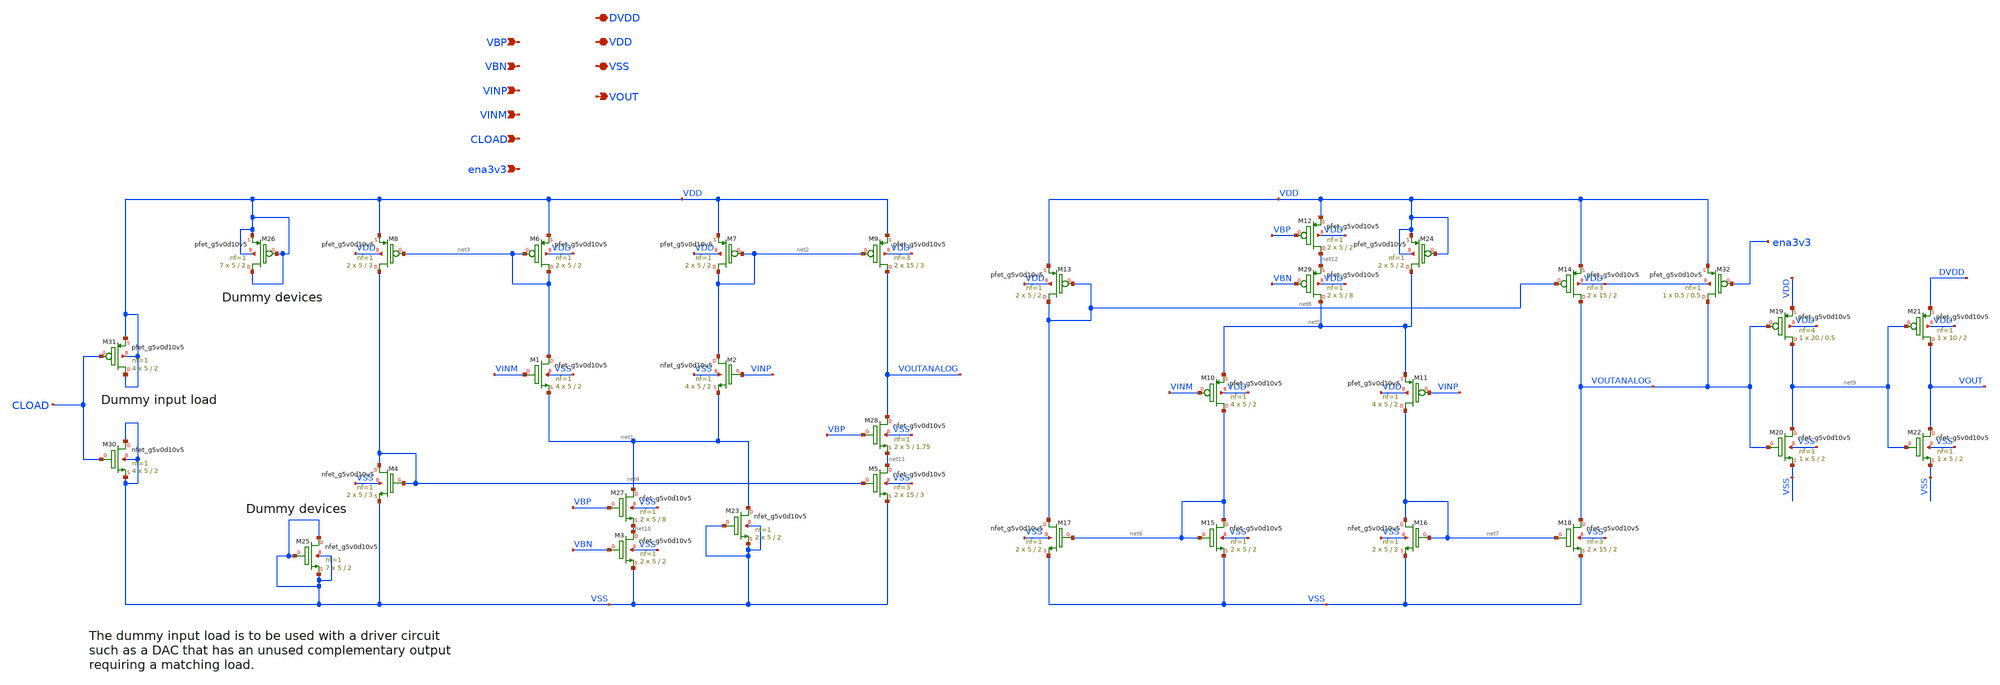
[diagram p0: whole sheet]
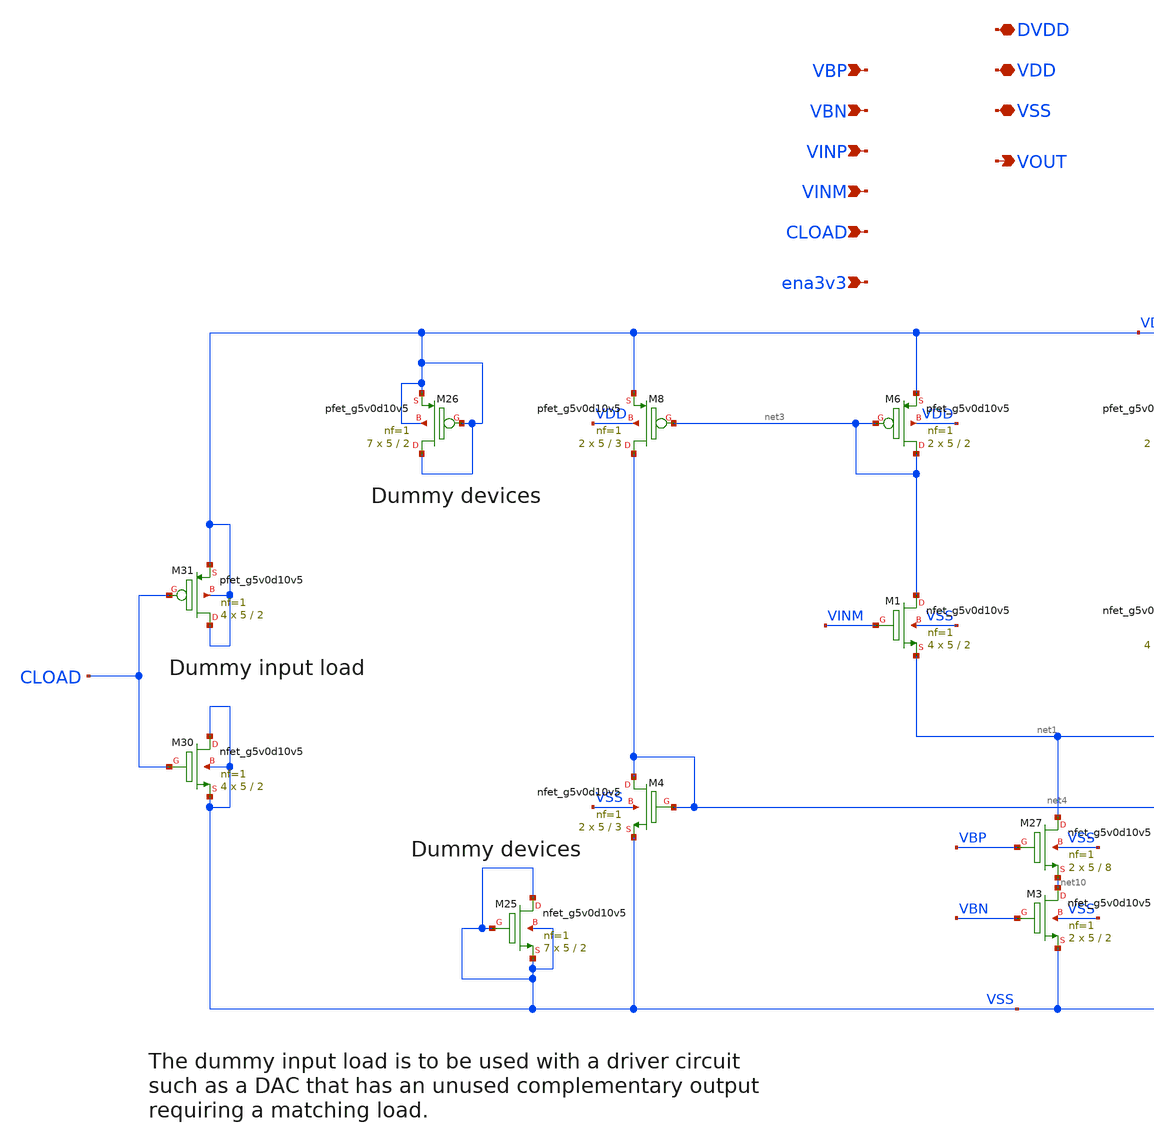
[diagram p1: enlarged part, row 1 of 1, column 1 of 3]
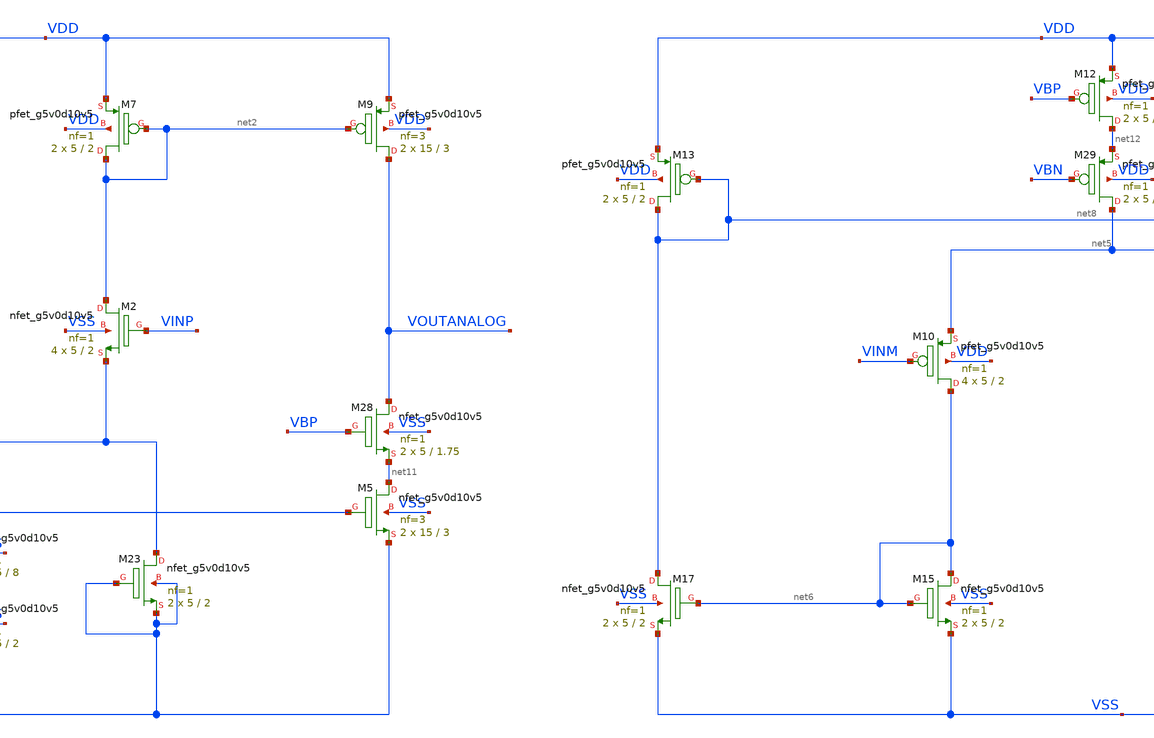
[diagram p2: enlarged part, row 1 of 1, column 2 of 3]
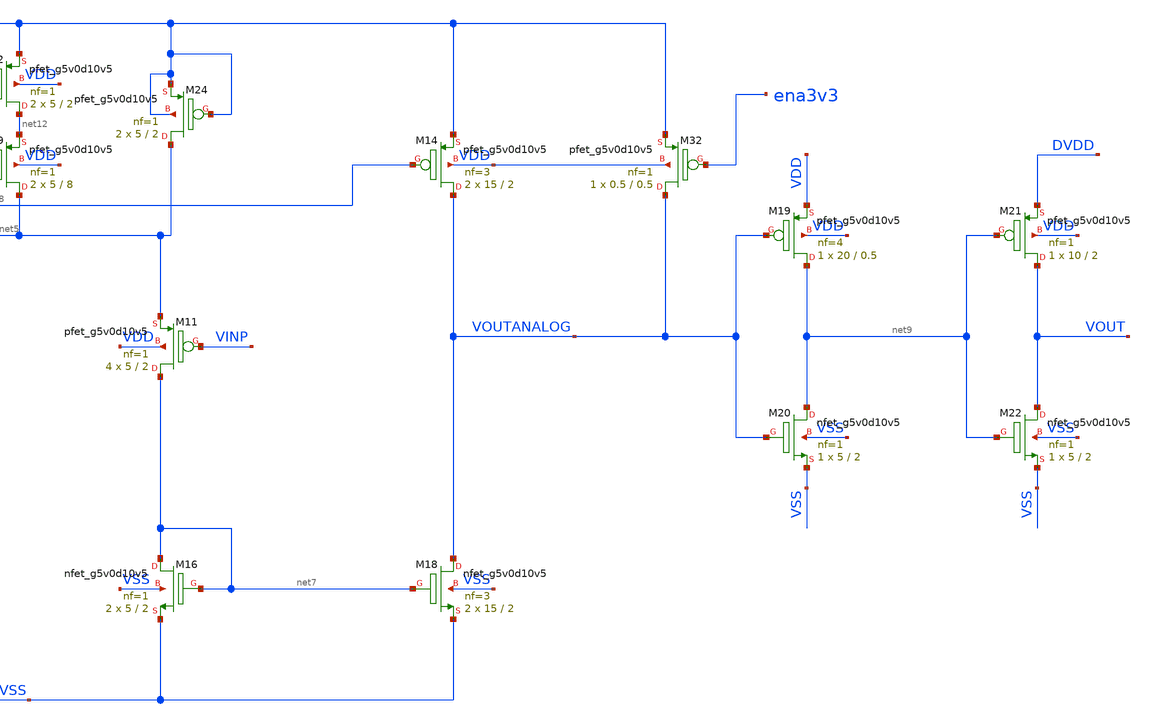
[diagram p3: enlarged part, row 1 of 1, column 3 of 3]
** sch_path: xschem/comparator_core_cload.sch
**.subckt comparator_core_cload VINP VINM VBN VBP VDD VSS VOUT DVDD CLOAD ena3v3
*.ipin VINP
*.ipin VINM
*.ipin VBN
*.ipin VBP
*.iopin VDD
*.iopin VSS
*.opin VOUT
*.iopin DVDD
*.ipin CLOAD
*.ipin ena3v3
XM3 net10 VBN VSS VSS sky130_fd_pr__nfet_g5v0d10v5 L=2 W=5 nf=1 ad='int((nf+1)/2) * W/nf * 0.29' as='int((nf+2)/2) * W/nf * 0.29'
+ pd='2*int((nf+1)/2) * (W/nf + 0.29)' ps='2*int((nf+2)/2) * (W/nf + 0.29)' nrd='0.29 / W' nrs='0.29 / W'
+ sa=0 sb=0 sd=0 mult=2 m=2
XM4 net4 net4 VSS VSS sky130_fd_pr__nfet_g5v0d10v5 L=3 W=5 nf=1 ad='int((nf+1)/2) * W/nf * 0.29' as='int((nf+2)/2) * W/nf * 0.29'
+ pd='2*int((nf+1)/2) * (W/nf + 0.29)' ps='2*int((nf+2)/2) * (W/nf + 0.29)' nrd='0.29 / W' nrs='0.29 / W'
+ sa=0 sb=0 sd=0 mult=2 m=2
XM5 net11 net4 VSS VSS sky130_fd_pr__nfet_g5v0d10v5 L=3 W=15 nf=3 ad='int((nf+1)/2) * W/nf * 0.29' as='int((nf+2)/2) * W/nf * 0.29'
+ pd='2*int((nf+1)/2) * (W/nf + 0.29)' ps='2*int((nf+2)/2) * (W/nf + 0.29)' nrd='0.29 / W' nrs='0.29 / W'
+ sa=0 sb=0 sd=0 mult=2 m=2
XM6 net3 net3 VDD VDD sky130_fd_pr__pfet_g5v0d10v5 L=2 W=5 nf=1 ad='int((nf+1)/2) * W/nf * 0.29' as='int((nf+2)/2) * W/nf * 0.29'
+ pd='2*int((nf+1)/2) * (W/nf + 0.29)' ps='2*int((nf+2)/2) * (W/nf + 0.29)' nrd='0.29 / W' nrs='0.29 / W'
+ sa=0 sb=0 sd=0 mult=2 m=2
XM7 net2 net2 VDD VDD sky130_fd_pr__pfet_g5v0d10v5 L=2 W=5 nf=1 ad='int((nf+1)/2) * W/nf * 0.29' as='int((nf+2)/2) * W/nf * 0.29'
+ pd='2*int((nf+1)/2) * (W/nf + 0.29)' ps='2*int((nf+2)/2) * (W/nf + 0.29)' nrd='0.29 / W' nrs='0.29 / W'
+ sa=0 sb=0 sd=0 mult=2 m=2
XM8 net4 net3 VDD VDD sky130_fd_pr__pfet_g5v0d10v5 L=3 W=5 nf=1 ad='int((nf+1)/2) * W/nf * 0.29' as='int((nf+2)/2) * W/nf * 0.29'
+ pd='2*int((nf+1)/2) * (W/nf + 0.29)' ps='2*int((nf+2)/2) * (W/nf + 0.29)' nrd='0.29 / W' nrs='0.29 / W'
+ sa=0 sb=0 sd=0 mult=2 m=2
XM9 VOUTANALOG net2 VDD VDD sky130_fd_pr__pfet_g5v0d10v5 L=3 W=15 nf=3 ad='int((nf+1)/2) * W/nf * 0.29'
+ as='int((nf+2)/2) * W/nf * 0.29' pd='2*int((nf+1)/2) * (W/nf + 0.29)' ps='2*int((nf+2)/2) * (W/nf + 0.29)'
+ nrd='0.29 / W' nrs='0.29 / W' sa=0 sb=0 sd=0 mult=2 m=2
XM10 net6 VINM net5 VDD sky130_fd_pr__pfet_g5v0d10v5 L=2 W=5 nf=1 ad='int((nf+1)/2) * W/nf * 0.29' as='int((nf+2)/2) * W/nf * 0.29'
+ pd='2*int((nf+1)/2) * (W/nf + 0.29)' ps='2*int((nf+2)/2) * (W/nf + 0.29)' nrd='0.29 / W' nrs='0.29 / W'
+ sa=0 sb=0 sd=0 mult=4 m=4
XM11 net7 VINP net5 VDD sky130_fd_pr__pfet_g5v0d10v5 L=2 W=5 nf=1 ad='int((nf+1)/2) * W/nf * 0.29' as='int((nf+2)/2) * W/nf * 0.29'
+ pd='2*int((nf+1)/2) * (W/nf + 0.29)' ps='2*int((nf+2)/2) * (W/nf + 0.29)' nrd='0.29 / W' nrs='0.29 / W'
+ sa=0 sb=0 sd=0 mult=4 m=4
XM12 net12 VBP VDD VDD sky130_fd_pr__pfet_g5v0d10v5 L=2 W=5 nf=1 ad='int((nf+1)/2) * W/nf * 0.29' as='int((nf+2)/2) * W/nf * 0.29'
+ pd='2*int((nf+1)/2) * (W/nf + 0.29)' ps='2*int((nf+2)/2) * (W/nf + 0.29)' nrd='0.29 / W' nrs='0.29 / W'
+ sa=0 sb=0 sd=0 mult=2 m=2
XM13 net8 net8 VDD VDD sky130_fd_pr__pfet_g5v0d10v5 L=2 W=5 nf=1 ad='int((nf+1)/2) * W/nf * 0.29' as='int((nf+2)/2) * W/nf * 0.29'
+ pd='2*int((nf+1)/2) * (W/nf + 0.29)' ps='2*int((nf+2)/2) * (W/nf + 0.29)' nrd='0.29 / W' nrs='0.29 / W'
+ sa=0 sb=0 sd=0 mult=2 m=2
XM14 VOUTANALOG net8 VDD VDD sky130_fd_pr__pfet_g5v0d10v5 L=2 W=15 nf=3 ad='int((nf+1)/2) * W/nf * 0.29'
+ as='int((nf+2)/2) * W/nf * 0.29' pd='2*int((nf+1)/2) * (W/nf + 0.29)' ps='2*int((nf+2)/2) * (W/nf + 0.29)'
+ nrd='0.29 / W' nrs='0.29 / W' sa=0 sb=0 sd=0 mult=2 m=2
XM15 net6 net6 VSS VSS sky130_fd_pr__nfet_g5v0d10v5 L=2 W=5 nf=1 ad='int((nf+1)/2) * W/nf * 0.29' as='int((nf+2)/2) * W/nf * 0.29'
+ pd='2*int((nf+1)/2) * (W/nf + 0.29)' ps='2*int((nf+2)/2) * (W/nf + 0.29)' nrd='0.29 / W' nrs='0.29 / W'
+ sa=0 sb=0 sd=0 mult=2 m=2
XM16 net7 net7 VSS VSS sky130_fd_pr__nfet_g5v0d10v5 L=2 W=5 nf=1 ad='int((nf+1)/2) * W/nf * 0.29' as='int((nf+2)/2) * W/nf * 0.29'
+ pd='2*int((nf+1)/2) * (W/nf + 0.29)' ps='2*int((nf+2)/2) * (W/nf + 0.29)' nrd='0.29 / W' nrs='0.29 / W'
+ sa=0 sb=0 sd=0 mult=2 m=2
XM17 net8 net6 VSS VSS sky130_fd_pr__nfet_g5v0d10v5 L=2 W=5 nf=1 ad='int((nf+1)/2) * W/nf * 0.29' as='int((nf+2)/2) * W/nf * 0.29'
+ pd='2*int((nf+1)/2) * (W/nf + 0.29)' ps='2*int((nf+2)/2) * (W/nf + 0.29)' nrd='0.29 / W' nrs='0.29 / W'
+ sa=0 sb=0 sd=0 mult=2 m=2
XM18 VOUTANALOG net7 VSS VSS sky130_fd_pr__nfet_g5v0d10v5 L=2 W=15 nf=3 ad='int((nf+1)/2) * W/nf * 0.29'
+ as='int((nf+2)/2) * W/nf * 0.29' pd='2*int((nf+1)/2) * (W/nf + 0.29)' ps='2*int((nf+2)/2) * (W/nf + 0.29)'
+ nrd='0.29 / W' nrs='0.29 / W' sa=0 sb=0 sd=0 mult=2 m=2
XM19 net9 VOUTANALOG VDD VDD sky130_fd_pr__pfet_g5v0d10v5 L=0.5 W=20 nf=4 ad='int((nf+1)/2) * W/nf * 0.29'
+ as='int((nf+2)/2) * W/nf * 0.29' pd='2*int((nf+1)/2) * (W/nf + 0.29)' ps='2*int((nf+2)/2) * (W/nf + 0.29)'
+ nrd='0.29 / W' nrs='0.29 / W' sa=0 sb=0 sd=0 mult=1 m=1
XM20 net9 VOUTANALOG VSS VSS sky130_fd_pr__nfet_g5v0d10v5 L=2 W=5 nf=1 ad='int((nf+1)/2) * W/nf * 0.29'
+ as='int((nf+2)/2) * W/nf * 0.29' pd='2*int((nf+1)/2) * (W/nf + 0.29)' ps='2*int((nf+2)/2) * (W/nf + 0.29)'
+ nrd='0.29 / W' nrs='0.29 / W' sa=0 sb=0 sd=0 mult=1 m=1
XM21 VOUT net9 DVDD VDD sky130_fd_pr__pfet_g5v0d10v5 L=2 W=10 nf=1 ad='int((nf+1)/2) * W/nf * 0.29' as='int((nf+2)/2) * W/nf * 0.29'
+ pd='2*int((nf+1)/2) * (W/nf + 0.29)' ps='2*int((nf+2)/2) * (W/nf + 0.29)' nrd='0.29 / W' nrs='0.29 / W'
+ sa=0 sb=0 sd=0 mult=1 m=1
XM22 VOUT net9 VSS VSS sky130_fd_pr__nfet_g5v0d10v5 L=2 W=5 nf=1 ad='int((nf+1)/2) * W/nf * 0.29' as='int((nf+2)/2) * W/nf * 0.29'
+ pd='2*int((nf+1)/2) * (W/nf + 0.29)' ps='2*int((nf+2)/2) * (W/nf + 0.29)' nrd='0.29 / W' nrs='0.29 / W'
+ sa=0 sb=0 sd=0 mult=1 m=1
XM23 net1 VSS VSS VSS sky130_fd_pr__nfet_g5v0d10v5 L=2 W=5 nf=1 ad='int((nf+1)/2) * W/nf * 0.29' as='int((nf+2)/2) * W/nf * 0.29'
+ pd='2*int((nf+1)/2) * (W/nf + 0.29)' ps='2*int((nf+2)/2) * (W/nf + 0.29)' nrd='0.29 / W' nrs='0.29 / W'
+ sa=0 sb=0 sd=0 mult=2 m=2
XM24 net5 VDD VDD VDD sky130_fd_pr__pfet_g5v0d10v5 L=2 W=5 nf=1 ad='int((nf+1)/2) * W/nf * 0.29' as='int((nf+2)/2) * W/nf * 0.29'
+ pd='2*int((nf+1)/2) * (W/nf + 0.29)' ps='2*int((nf+2)/2) * (W/nf + 0.29)' nrd='0.29 / W' nrs='0.29 / W'
+ sa=0 sb=0 sd=0 mult=2 m=2
XM25 VSS VSS VSS VSS sky130_fd_pr__nfet_g5v0d10v5 L=2 W=5 nf=1 ad='int((nf+1)/2) * W/nf * 0.29' as='int((nf+2)/2) * W/nf * 0.29'
+ pd='2*int((nf+1)/2) * (W/nf + 0.29)' ps='2*int((nf+2)/2) * (W/nf + 0.29)' nrd='0.29 / W' nrs='0.29 / W'
+ sa=0 sb=0 sd=0 mult=7 m=7
XM26 VDD VDD VDD VDD sky130_fd_pr__pfet_g5v0d10v5 L=2 W=5 nf=1 ad='int((nf+1)/2) * W/nf * 0.29' as='int((nf+2)/2) * W/nf * 0.29'
+ pd='2*int((nf+1)/2) * (W/nf + 0.29)' ps='2*int((nf+2)/2) * (W/nf + 0.29)' nrd='0.29 / W' nrs='0.29 / W'
+ sa=0 sb=0 sd=0 mult=7 m=7
XM1 net3 VINM net1 VSS sky130_fd_pr__nfet_g5v0d10v5 L=2 W=5 nf=1 ad='int((nf+1)/2) * W/nf * 0.29' as='int((nf+2)/2) * W/nf * 0.29'
+ pd='2*int((nf+1)/2) * (W/nf + 0.29)' ps='2*int((nf+2)/2) * (W/nf + 0.29)' nrd='0.29 / W' nrs='0.29 / W'
+ sa=0 sb=0 sd=0 mult=4 m=4
XM2 net2 VINP net1 VSS sky130_fd_pr__nfet_g5v0d10v5 L=2 W=5 nf=1 ad='int((nf+1)/2) * W/nf * 0.29' as='int((nf+2)/2) * W/nf * 0.29'
+ pd='2*int((nf+1)/2) * (W/nf + 0.29)' ps='2*int((nf+2)/2) * (W/nf + 0.29)' nrd='0.29 / W' nrs='0.29 / W'
+ sa=0 sb=0 sd=0 mult=4 m=4
XM27 net1 VBP net10 VSS sky130_fd_pr__nfet_g5v0d10v5 L=8 W=5 nf=1 ad='int((nf+1)/2) * W/nf * 0.29' as='int((nf+2)/2) * W/nf * 0.29'
+ pd='2*int((nf+1)/2) * (W/nf + 0.29)' ps='2*int((nf+2)/2) * (W/nf + 0.29)' nrd='0.29 / W' nrs='0.29 / W'
+ sa=0 sb=0 sd=0 mult=2 m=2
XM28 VOUTANALOG VBP net11 VSS sky130_fd_pr__nfet_g5v0d10v5 L=1.75 W=5 nf=1 ad='int((nf+1)/2) * W/nf * 0.29'
+ as='int((nf+2)/2) * W/nf * 0.29' pd='2*int((nf+1)/2) * (W/nf + 0.29)' ps='2*int((nf+2)/2) * (W/nf + 0.29)'
+ nrd='0.29 / W' nrs='0.29 / W' sa=0 sb=0 sd=0 mult=2 m=2
XM29 net5 VBN net12 VDD sky130_fd_pr__pfet_g5v0d10v5 L=8 W=5 nf=1 ad='int((nf+1)/2) * W/nf * 0.29' as='int((nf+2)/2) * W/nf * 0.29'
+ pd='2*int((nf+1)/2) * (W/nf + 0.29)' ps='2*int((nf+2)/2) * (W/nf + 0.29)' nrd='0.29 / W' nrs='0.29 / W'
+ sa=0 sb=0 sd=0 mult=2 m=2
XM30 VSS CLOAD VSS VSS sky130_fd_pr__nfet_g5v0d10v5 L=2 W=5 nf=1 ad='int((nf+1)/2) * W/nf * 0.29' as='int((nf+2)/2) * W/nf * 0.29'
+ pd='2*int((nf+1)/2) * (W/nf + 0.29)' ps='2*int((nf+2)/2) * (W/nf + 0.29)' nrd='0.29 / W' nrs='0.29 / W'
+ sa=0 sb=0 sd=0 mult=4 m=4
XM31 VDD CLOAD VDD VDD sky130_fd_pr__pfet_g5v0d10v5 L=2 W=5 nf=1 ad='int((nf+1)/2) * W/nf * 0.29' as='int((nf+2)/2) * W/nf * 0.29'
+ pd='2*int((nf+1)/2) * (W/nf + 0.29)' ps='2*int((nf+2)/2) * (W/nf + 0.29)' nrd='0.29 / W' nrs='0.29 / W'
+ sa=0 sb=0 sd=0 mult=4 m=4
XM32 VOUTANALOG ena3v3 VDD VDD sky130_fd_pr__pfet_g5v0d10v5 L=0.5 W=0.5 nf=1 ad='int((nf+1)/2) * W/nf * 0.29'
+ as='int((nf+2)/2) * W/nf * 0.29' pd='2*int((nf+1)/2) * (W/nf + 0.29)' ps='2*int((nf+2)/2) * (W/nf + 0.29)'
+ nrd='0.29 / W' nrs='0.29 / W' sa=0 sb=0 sd=0 mult=1 m=1
**.ends
.end
